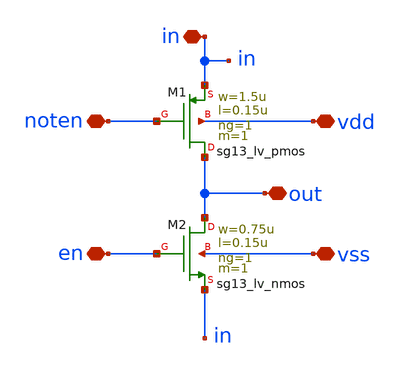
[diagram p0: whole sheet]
** sch_path: design/blocks/transmissiongate/schematic/transmissiongate.sch
**.subckt transmissiongate noten en in out vdd vss
*.iopin noten
*.iopin en
*.iopin in
*.iopin out
*.iopin vdd
*.iopin vss
XM1 out noten in vdd sg13_lv_pmos w=1.5u l=0.15u ng=1 m=1 mm_ok=1
XM2 out en in vss sg13_lv_nmos w=0.75u l=0.15u ng=1 m=1 mm_ok=1
**.ends
.end
